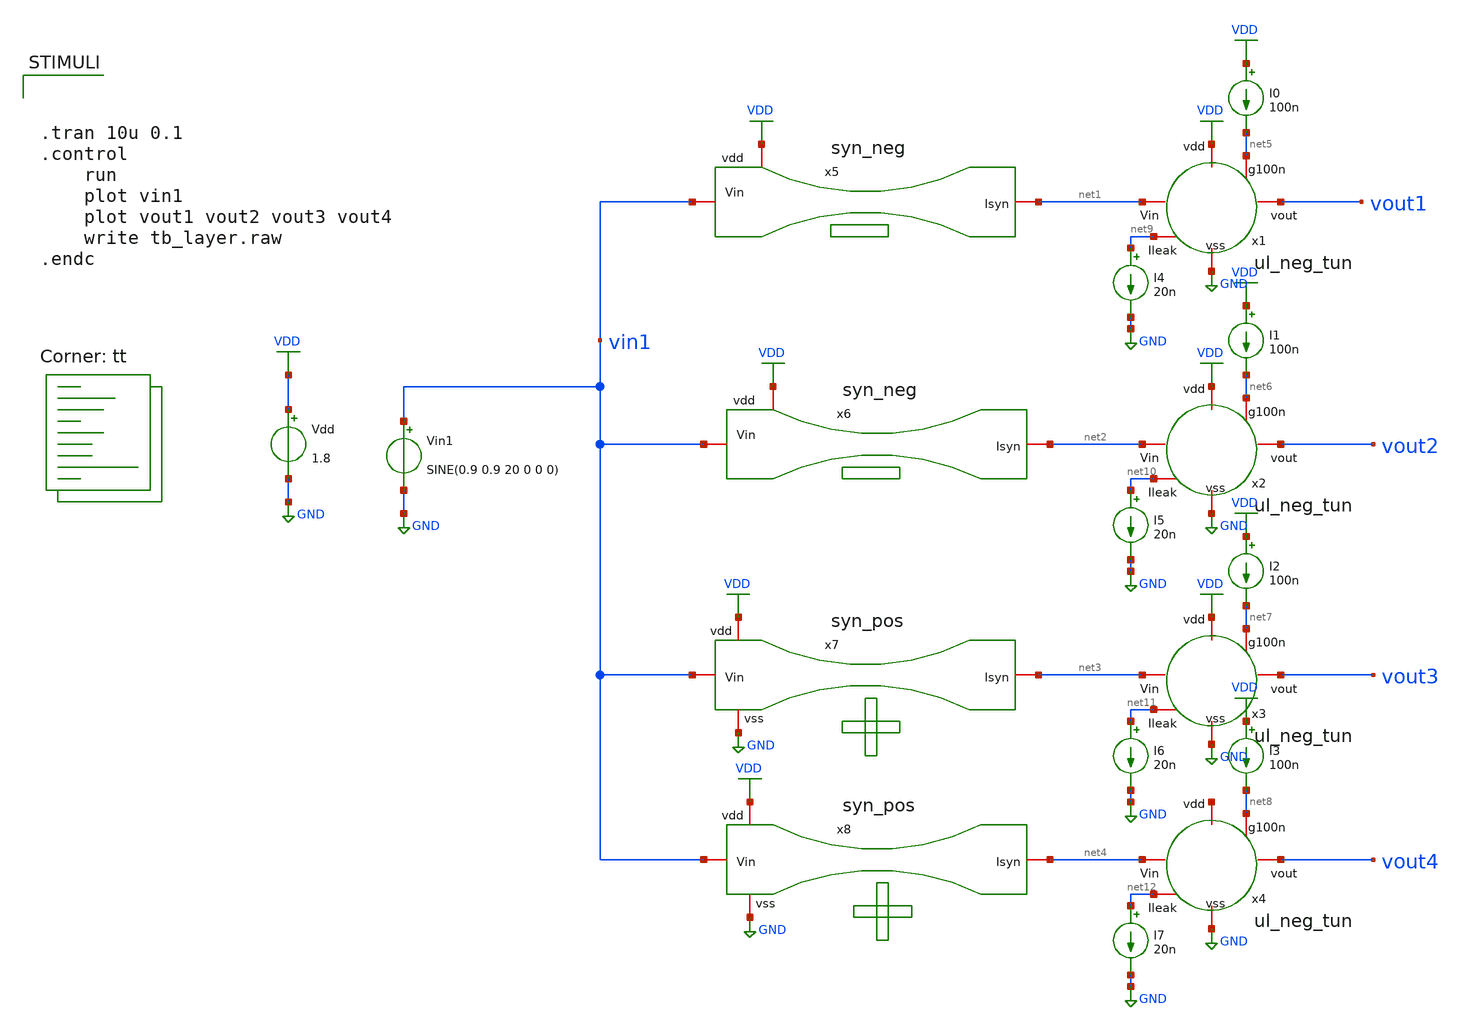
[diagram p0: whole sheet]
** sch_path: tb_layer.sch
**.subckt tb_layer
x1 net1 VDD net5 vout1 net9 GND ul_neg_tun
x2 net2 VDD net6 vout2 net10 GND ul_neg_tun
x3 net3 VDD net7 vout3 net11 GND ul_neg_tun
x4 net4 net13 net8 vout4 net12 GND ul_neg_tun
x5 VDD vin1 net1 syn_neg
x6 VDD vin1 net2 syn_neg
x7 GND vin1 net3 VDD syn_pos
x8 GND vin1 net4 VDD syn_pos
Vdd VDD GND 1.8
Vin1 vin1 GND SINE(0.9 0.9 20 0 0 0)
I0 VDD net5 100n
I1 VDD net6 100n
I2 VDD net7 100n
I3 VDD net8 100n
I4 net9 GND 20n
I5 net10 GND 20n
I6 net11 GND 20n
I7 net12 GND 20n
**** begin user architecture code
.lib $::SKYWATER_MODELS/sky130.lib.spice tt
**** end user architecture code
**.ends

* expanding   symbol:  ul_neg_tun.sym # of pins=6
** sym_path: Neuron/ultralif/ul_neg_tun.sym
** sch_path: Neuron/ultralif/ul_neg_tun.sch
.subckt ul_neg_tun Iext vdd g100n vout Ileak vss
*.iopin Iext
*.iopin vout
*.iopin vss
*.iopin Ileak
*.iopin vdd
*.iopin g100n
XM1 Ileak Ileak vm vdd sky130_fd_pr__pfet_01v8 L=10 W=1 nf=1 ad='int((nf+1)/2) * W/nf * 0.29' as='int((nf+2)/2) * W/nf * 0.29'
+ pd='2*int((nf+1)/2) * (W/nf + 0.29)' ps='2*int((nf+2)/2) * (W/nf + 0.29)' nrd='0.29 / W' nrs='0.29 / W'
+ sa=0 sb=0 sd=0 mult=1 m=1
XM2 Ileak net1 vm vdd sky130_fd_pr__pfet_01v8 L=0.15 W=1.5 nf=1 ad='int((nf+1)/2) * W/nf * 0.29' as='int((nf+2)/2) * W/nf * 0.29'
+ pd='2*int((nf+1)/2) * (W/nf + 0.29)' ps='2*int((nf+2)/2) * (W/nf + 0.29)' nrd='0.29 / W' nrs='0.29 / W'
+ sa=0 sb=0 sd=0 mult=1 m=1
XM3 net1 net1 vm vdd sky130_fd_pr__pfet_01v8 L=0.15 W=15 nf=1 ad='int((nf+1)/2) * W/nf * 0.29' as='int((nf+2)/2) * W/nf * 0.29'
+ pd='2*int((nf+1)/2) * (W/nf + 0.29)' ps='2*int((nf+2)/2) * (W/nf + 0.29)' nrd='0.29 / W' nrs='0.29 / W'
+ sa=0 sb=0 sd=0 mult=1 m=1
XM4 net1 Ileak vss vss sky130_fd_pr__nfet_01v8 L=4 W=1 nf=1 ad='int((1 + 1)/2) * 1 / 1 * 0.29' as='int((1 + 2)/2) * 1 / 1 * 0.29'
+ pd='2*int((1 + 1)/2) * (1 / 1 + 0.29)' ps='2*int((1 + 2)/2) * (1 / 1 + 0.29)' nrd='0.29 / 1 ' nrs='0.29 / 1 '
+ sa=0 sb=0 sd=0 mult=1 m=1
C1 vm vss 1p m=1
XM5 vout_n Ileak vss vss sky130_fd_pr__nfet_01v8 L=0.15 W=1 nf=1 ad='int((1 + 1)/2) * 1 / 1 * 0.29' as='int((1 + 2)/2) * 1 / 1 * 0.29'
+ pd='2*int((1 + 1)/2) * (1 / 1 + 0.29)' ps='2*int((1 + 2)/2) * (1 / 1 + 0.29)' nrd='0.29 / 1 ' nrs='0.29 / 1 '
+ sa=0 sb=0 sd=0 mult=1 m=1
XM6 vout_n g100n vdd vdd sky130_fd_pr__pfet_01v8 L=0.15 W=2 nf=1 ad='int((nf+1)/2) * W/nf * 0.29' as='int((nf+2)/2) * W/nf * 0.29'
+ pd='2*int((nf+1)/2) * (W/nf + 0.29)' ps='2*int((nf+2)/2) * (W/nf + 0.29)' nrd='0.29 / W' nrs='0.29 / W'
+ sa=0 sb=0 sd=0 mult=1 m=1
XM7 vout vout_n vss vss sky130_fd_pr__nfet_01v8 L=0.15 W=1 nf=1 ad='int((1 + 1)/2) * 1 / 1 * 0.29' as='int((1 + 2)/2) * 1 / 1 * 0.29'
+ pd='2*int((1 + 1)/2) * (1 / 1 + 0.29)' ps='2*int((1 + 2)/2) * (1 / 1 + 0.29)' nrd='0.29 / 1 ' nrs='0.29 / 1 '
+ sa=0 sb=0 sd=0 mult=1 m=1
XM8 vout vout_n vdd vdd sky130_fd_pr__pfet_01v8 L=0.15 W=2 nf=1 ad='int((nf+1)/2) * W/nf * 0.29' as='int((nf+2)/2) * W/nf * 0.29'
+ pd='2*int((nf+1)/2) * (W/nf + 0.29)' ps='2*int((nf+2)/2) * (W/nf + 0.29)' nrd='0.29 / W' nrs='0.29 / W'
+ sa=0 sb=0 sd=0 mult=1 m=1
XM9 vm Ileak Iext vdd sky130_fd_pr__pfet_01v8 L=0.15 W=2 nf=1 ad='int((nf+1)/2) * W/nf * 0.29' as='int((nf+2)/2) * W/nf * 0.29'
+ pd='2*int((nf+1)/2) * (W/nf + 0.29)' ps='2*int((nf+2)/2) * (W/nf + 0.29)' nrd='0.29 / W' nrs='0.29 / W'
+ sa=0 sb=0 sd=0 mult=1 m=1
.ends


* expanding   symbol:  syn_neg.sym # of pins=3
** sym_path: Neuron/ultralif/syn_neg.sym
** sch_path: Neuron/ultralif/syn_neg.sch
.subckt syn_neg vdd Vin Isyn
*.iopin Vin
*.iopin Isyn
*.iopin vdd
XM10 Isyn Vin vx vdd sky130_fd_pr__pfet_01v8 L=30 W=0.5 nf=1 ad='int((nf+1)/2) * W/nf * 0.29' as='int((nf+2)/2) * W/nf * 0.29'
+ pd='2*int((nf+1)/2) * (W/nf + 0.29)' ps='2*int((nf+2)/2) * (W/nf + 0.29)' nrd='0.29 / W' nrs='0.29 / W'
+ sa=0 sb=0 sd=0 mult=1 m=1
XM1 vx Vin vdd vdd sky130_fd_pr__pfet_01v8 L=30 W=0.5 nf=1 ad='int((nf+1)/2) * W/nf * 0.29' as='int((nf+2)/2) * W/nf * 0.29'
+ pd='2*int((nf+1)/2) * (W/nf + 0.29)' ps='2*int((nf+2)/2) * (W/nf + 0.29)' nrd='0.29 / W' nrs='0.29 / W'
+ sa=0 sb=0 sd=0 mult=1 m=1
.ends


* expanding   symbol:  syn_pos.sym # of pins=4
** sym_path: Neuron/ultralif/syn_pos.sym
** sch_path: Neuron/ultralif/syn_pos.sch
.subckt syn_pos vss Vin Isyn vdd
*.iopin Vin
*.iopin vdd
*.iopin vss
*.iopin Isyn
XM9 Isyn vx vdd vdd sky130_fd_pr__pfet_01v8 L=1 W=0.5 nf=1 ad='int((nf+1)/2) * W/nf * 0.29' as='int((nf+2)/2) * W/nf * 0.29'
+ pd='2*int((nf+1)/2) * (W/nf + 0.29)' ps='2*int((nf+2)/2) * (W/nf + 0.29)' nrd='0.29 / W' nrs='0.29 / W'
+ sa=0 sb=0 sd=0 mult=1 m=1
XM10 vx vx vdd vdd sky130_fd_pr__pfet_01v8 L=0.15 W=0.5 nf=1 ad='int((nf+1)/2) * W/nf * 0.29' as='int((nf+2)/2) * W/nf * 0.29'
+ pd='2*int((nf+1)/2) * (W/nf + 0.29)' ps='2*int((nf+2)/2) * (W/nf + 0.29)' nrd='0.29 / W' nrs='0.29 / W'
+ sa=0 sb=0 sd=0 mult=5 m=5
XM12 vx Vin vss vss sky130_fd_pr__nfet_01v8 L=1 W=0.4 nf=1 ad='int((1 + 1)/2) * 0.4 / 1 * 0.29' as='int((1 + 2)/2) * 0.4 / 1 * 0.29'
+ pd='2*int((1 + 1)/2) * (0.4 / 1 + 0.29)' ps='2*int((1 + 2)/2) * (0.4 / 1 + 0.29)' nrd='0.29 / 0.4 ' nrs='0.29 / 0.4 '
+ sa=0 sb=0 sd=0 mult=1 m=1
.ends

.GLOBAL GND
.GLOBAL VDD
**** begin user architecture code



.tran 10u 0.1
.control
	run
	plot vin1
	plot vout1 vout2 vout3 vout4
	write tb_layer.raw
.endc


**** end user architecture code
.end
